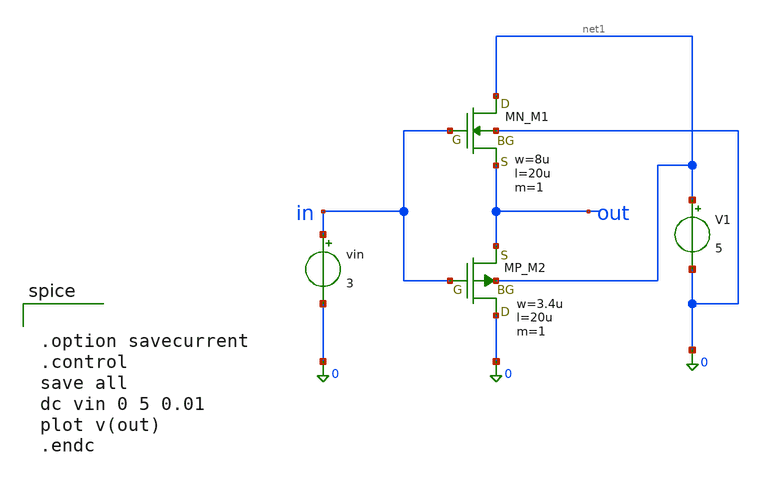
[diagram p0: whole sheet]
** sch_path: member_project/JJY_Receiver/Masahiro/jjy_recv/buffer/class_b_pushpull.sch
**.subckt class_b_pushpull
XM1 net1 in out 0 NMOS w=8u l=20u as=0 ad=0 ps=0 pd=0 nrd=0 nrs=0 m=1
XM2 0 in out net1 PMOS w=3.4u l=20u as=0 ad=0 ps=0 pd=0 nrd=0 nrs=0 m=1
V1 net1 0 5
vin in 0 3
**** begin user architecture code
 .include $::LIB/ip62_models


.option savecurrent
.control
save all
dc vin 0 5 0.01
plot v(out)
.endc


**** end user architecture code
**.ends
.end
